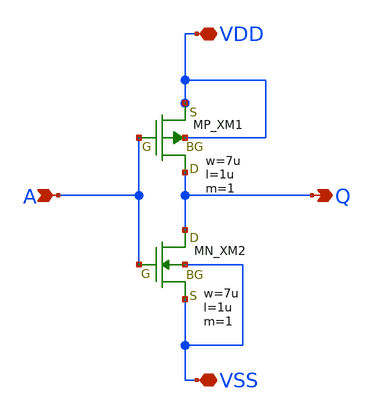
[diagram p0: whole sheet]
** sch_path: schematic/20250924_OSS_Workshop/Qdai/inverter_MUX_02/inv_nakabuchi.sch
**.subckt inv_nakabuchi VDD Q VSS A
*.iopin VDD
*.opin Q
*.iopin VSS
*.ipin A
XM1 Q A VDD VDD PMOS w=7u l=1u as=0 ad=0 ps=0 pd=0 nrd=0 nrs=0 m=1
XM2 Q A VSS VSS NMOS w=7u l=1u as=0 ad=0 ps=0 pd=0 nrd=0 nrs=0 m=1
**.ends
.end
